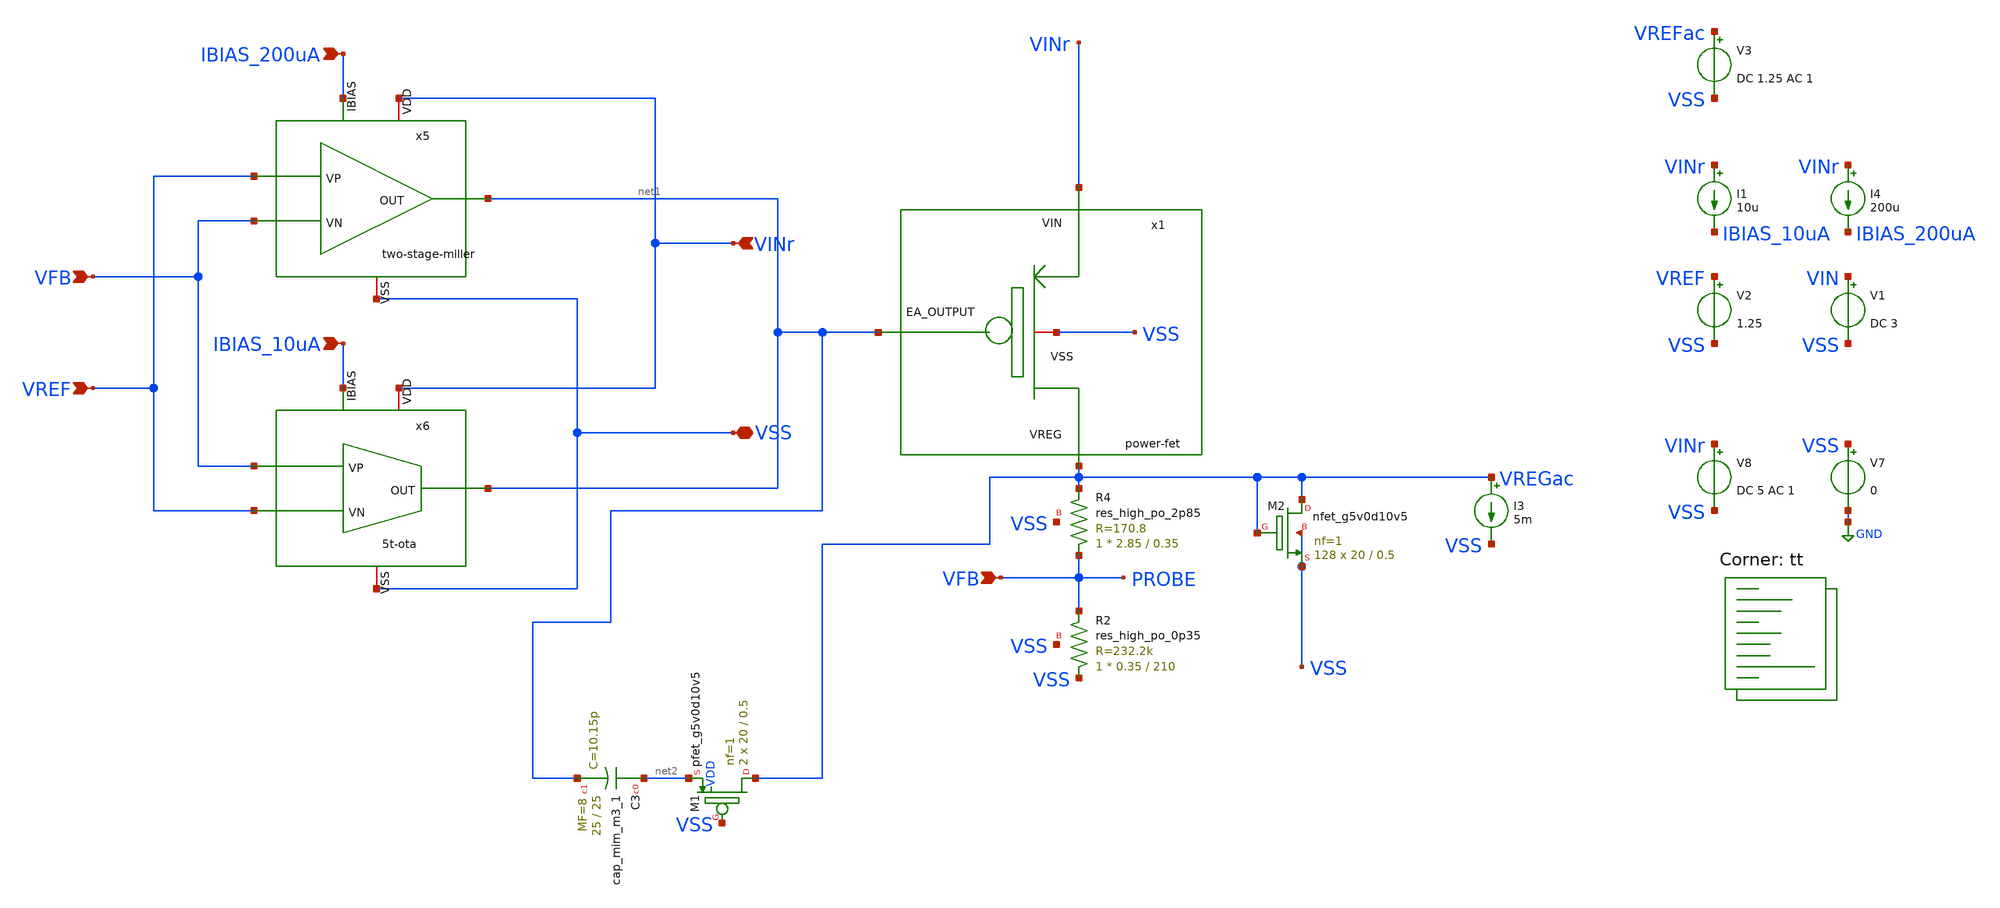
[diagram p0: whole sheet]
** sch_path: bandgap/testbench/ldo-psrr.sch
**.subckt ldo-psrr VFB VREF IBIAS_10uA IBIAS_200uA VINr VSS VFB
*.ipin VFB
*.ipin VREF
*.ipin IBIAS_10uA
*.ipin IBIAS_200uA
*.ipin VINr
*.iopin VSS
*.ipin VFB
V2 VREF VSS 1.25
V7 VSS GND 0
V8 VINr VSS DC 5 AC 1
I4 VINr IBIAS_200uA 200u
I1 VINr IBIAS_10uA 10u
XR4 VFB VREGac VSS sky130_fd_pr__res_high_po_2p85 L=0.35 mult=1 m=1
x5 VINr net1 VREF VFB IBIAS_200uA VSS two-stage-miller
x6 VINr net1 IBIAS_10uA VREF VFB VSS 5t-ota
I3 VREGac VSS 5m
V1 VIN VSS DC 3
XR2 VSS VFB VSS sky130_fd_pr__res_high_po_0p35 L=210 mult=1 m=1
V3 VREFac VSS DC 1.25 AC 1
XC3 net2 net1 sky130_fd_pr__cap_mim_m3_1 W=25 L=25 MF=8 m=8
XM2 VREGac VREGac VSS VSS sky130_fd_pr__nfet_g5v0d10v5 L=0.5 W=20 nf=1 ad='int((nf+1)/2) * W/nf * 0.29'
+ as='int((nf+2)/2) * W/nf * 0.29' pd='2*int((nf+1)/2) * (W/nf + 0.29)' ps='2*int((nf+2)/2) * (W/nf + 0.29)'
+ nrd='0.29 / W' nrs='0.29 / W' sa=0 sb=0 sd=0 mult=128 m=128
XM1 VREGac VSS net2 VDD sky130_fd_pr__pfet_g5v0d10v5 L=0.5 W=20 nf=1 ad='int((nf+1)/2) * W/nf * 0.29'
+ as='int((nf+2)/2) * W/nf * 0.29' pd='2*int((nf+1)/2) * (W/nf + 0.29)' ps='2*int((nf+2)/2) * (W/nf + 0.29)'
+ nrd='0.29 / W' nrs='0.29 / W' sa=0 sb=0 sd=0 mult=2 m=2
x1 VINr VSS net1 VREGac power-fet
**** begin user architecture code


.temp 27
.control
    * Lakukan simulasi AC
    AC DEC 100 1 100G

    * 1. Menghitung PSRR yang Benar
    * PSRR = Gain dari Supply ke Output (VREG).
    * Biasanya kita ingin melihat penolakan (rejection), jadi kita hitung 1/Gain.
    * Jika input AC supply (Vripple) = 1V, maka PSRR_db = -db(v(VREGac))
    let psrr_plot = -db(v(VREGac))

    * 2. Menghitung Loop Gain & Phase Margin
    * Pastikan v(PROBE) adalah node setelah injeksi AC (Tian Method / Middlebrook)
    let loop_gain_complex = v(PROBE)
    let lg_db = db(loop_gain_complex)
    * ph(x) di ngspice hasilnya dalam radian, kita ubah ke derajat
    let lg_ph = ph(loop_gain_complex) * 180 / PI

    * Phase Margin biasanya diukur dari jarak fase ke -180 derajat
    let phase_margin_plot = lg_ph + 180

    * 3. Pengukuran Otomatis (MEAS)
    * Cari Unity Gain Frequency (UGF)
    meas ac f_unity when lg_db=0

    * Cari Phase Margin pada frekuensi f_unity tersebut
    * Gunakan 'at' dengan variabel yang sudah didapat dari f_unity
    meas ac PM_value find phase_margin_plot at=f_unity

    * 4. Menghitung PSRR pada Berbagai Band
    * Ingat: Gunakan let psrr_plot yang sudah didefinisikan agar tidak redundan
    meas ac psrr_dc find psrr_plot at=1
    meas ac psrr_100k find psrr_plot at=100k
    meas ac psrr_1M find psrr_plot at=1meg

    * 5. Cetak Hasil ke Terminal
    echo ======================================
    echo Unity Gain Frequency: $&f_unity Hz
    echo Phase Margin: $&PM_value degrees
    echo PSRR at DC: $&psrr_dc dB
    echo PSRR at 100kHz: $&psrr_100k dB
    echo PSRR at 1MHz: $&psrr_1M dB
    echo ======================================

    * 6. Plotting
    plot lg_db phase_margin_plot ylimit -50 100 title 'Loop Gain and Phase'
    plot psrr_plot title 'Power Supply Rejection Ratio (dB)'

.endc


.lib $::SKYWATER_MODELS/sky130.lib.spice tt
**** end user architecture code
**.ends
.GLOBAL GND
.end
